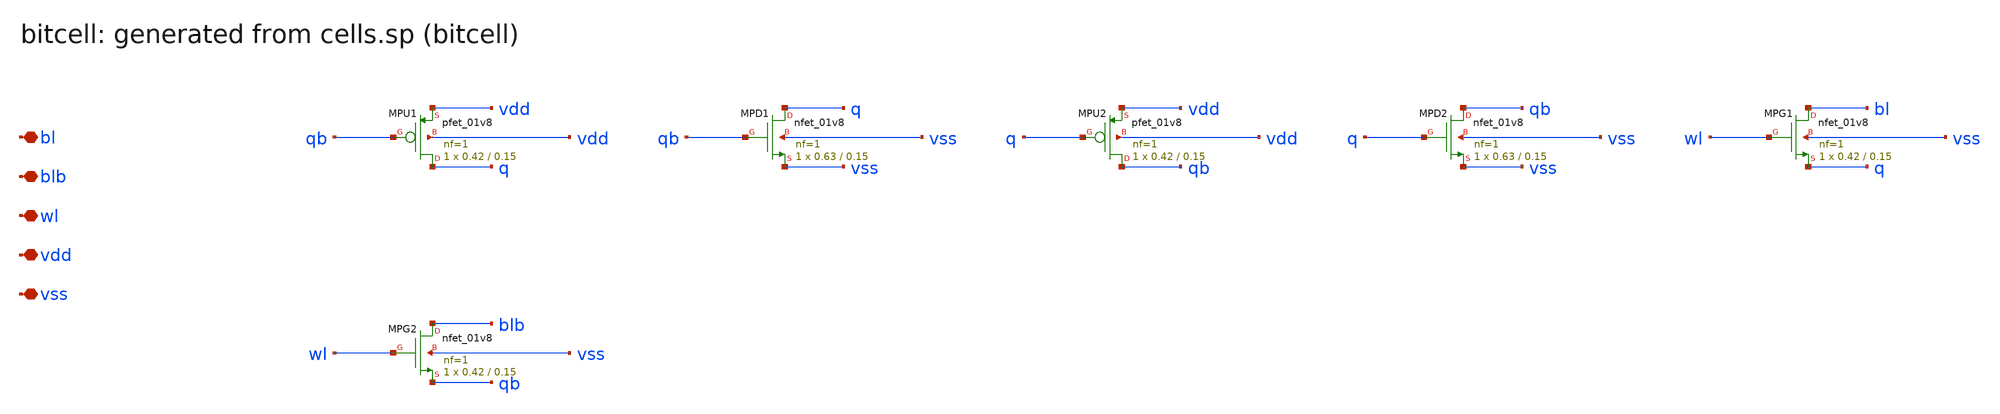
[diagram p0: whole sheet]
** sch_path: sram/xschem/bitcell.sch
**.subckt bitcell bl blb wl vdd vss
*.iopin bl
*.iopin blb
*.iopin wl
*.iopin vdd
*.iopin vss
XMPU1 q qb vdd vdd sky130_fd_pr__pfet_01v8 L=0.15 W=0.42 nf=1 ad='int((nf+1)/2) * W/nf * 0.29' as='int((nf+2)/2) * W/nf * 0.29'
+ pd='2*int((nf+1)/2) * (W/nf + 0.29)' ps='2*int((nf+2)/2) * (W/nf + 0.29)' nrd='0.29 / W' nrs='0.29 / W'
+ sa=0 sb=0 sd=0 mult=1 m=1
XMPD1 q qb vss vss sky130_fd_pr__nfet_01v8 L=0.15 W=0.63 nf=1 ad='int((1 + 1)/2) * 0.63 / 1 * 0.29' as='int((1 + 2)/2) * 0.63 / 1 * 0.29'
+ pd='2*int((1 + 1)/2) * (0.63 / 1 + 0.29)' ps='2*int((1 + 2)/2) * (0.63 / 1 + 0.29)' nrd='0.29 / 0.63 '
+ nrs='0.29 / 0.63 ' sa=0 sb=0 sd=0 mult=1 m=1
XMPU2 qb q vdd vdd sky130_fd_pr__pfet_01v8 L=0.15 W=0.42 nf=1 ad='int((nf+1)/2) * W/nf * 0.29' as='int((nf+2)/2) * W/nf * 0.29'
+ pd='2*int((nf+1)/2) * (W/nf + 0.29)' ps='2*int((nf+2)/2) * (W/nf + 0.29)' nrd='0.29 / W' nrs='0.29 / W'
+ sa=0 sb=0 sd=0 mult=1 m=1
XMPD2 qb q vss vss sky130_fd_pr__nfet_01v8 L=0.15 W=0.63 nf=1 ad='int((1 + 1)/2) * 0.63 / 1 * 0.29' as='int((1 + 2)/2) * 0.63 / 1 * 0.29'
+ pd='2*int((1 + 1)/2) * (0.63 / 1 + 0.29)' ps='2*int((1 + 2)/2) * (0.63 / 1 + 0.29)' nrd='0.29 / 0.63 '
+ nrs='0.29 / 0.63 ' sa=0 sb=0 sd=0 mult=1 m=1
XMPG1 bl wl q vss sky130_fd_pr__nfet_01v8 L=0.15 W=0.42 nf=1 ad='int((1 + 1)/2) * 0.42 / 1 * 0.29' as='int((1 + 2)/2) * 0.42 / 1 * 0.29'
+ pd='2*int((1 + 1)/2) * (0.42 / 1 + 0.29)' ps='2*int((1 + 2)/2) * (0.42 / 1 + 0.29)' nrd='0.29 / 0.42 '
+ nrs='0.29 / 0.42 ' sa=0 sb=0 sd=0 mult=1 m=1
XMPG2 blb wl qb vss sky130_fd_pr__nfet_01v8 L=0.15 W=0.42 nf=1 ad='int((1 + 1)/2) * 0.42 / 1 * 0.29'
+ as='int((1 + 2)/2) * 0.42 / 1 * 0.29' pd='2*int((1 + 1)/2) * (0.42 / 1 + 0.29)' ps='2*int((1 + 2)/2) * (0.42 / 1 + 0.29)'
+ nrd='0.29 / 0.42 ' nrs='0.29 / 0.42 ' sa=0 sb=0 sd=0 mult=1 m=1
**.ends
.end
